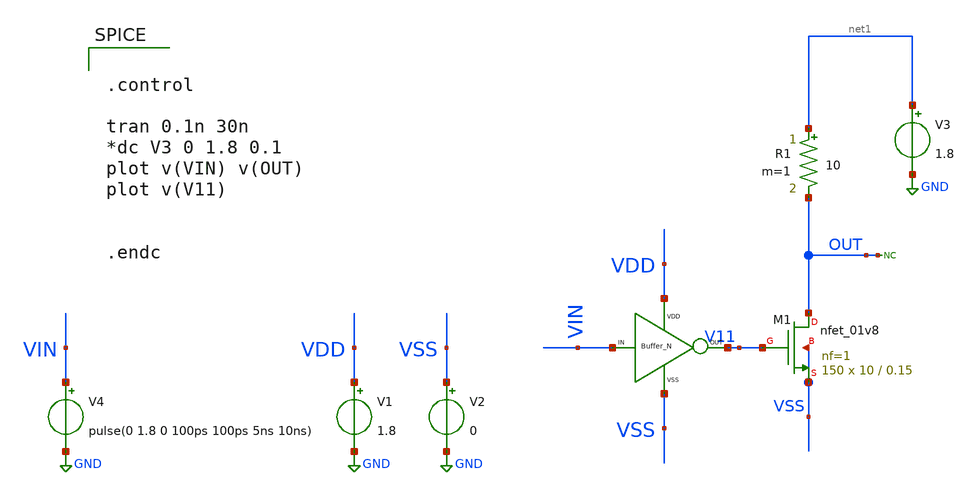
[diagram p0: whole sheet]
** sch_path: xschem/DC_DC_Converter_xschem/OTHERS/DC_DC_Converter_V7/BUFFER/BUFFER_NMOS/BUFFER_N_TB.sch
**.subckt BUFFER_N_TB
XM1 OUT V11 VSS VSS sky130_fd_pr__nfet_01v8 L=0.15 W=10 nf=1 ad='int((nf+1)/2) * W/nf * 0.29' as='int((nf+2)/2) * W/nf * 0.29'
+ pd='2*int((nf+1)/2) * (W/nf + 0.29)' ps='2*int((nf+2)/2) * (W/nf + 0.29)' nrd='0.29 / W' nrs='0.29 / W'
+ sa=0 sb=0 sd=0 mult=150 m=150
V1 VDD GND 1.8
V2 VSS GND 0
* noconn OUT
V4 VIN GND pulse(0 1.8 0 100ps 100ps 5ns 10ns)
V3 net1 GND 1.8
R1 net1 OUT 10 m=1
X2 VIN V11 VDD VSS BUFFER_N
**** begin user architecture code

** opencircuitdesign pdks install
.lib $::SKYWATER_MODELS/sky130.lib.spice tt




.control

tran 0.1n 30n
*dc V3 0 1.8 0.1
plot v(VIN) v(OUT)
plot v(V11)


.endc


**** end user architecture code
**.ends
.GLOBAL GND
.end
